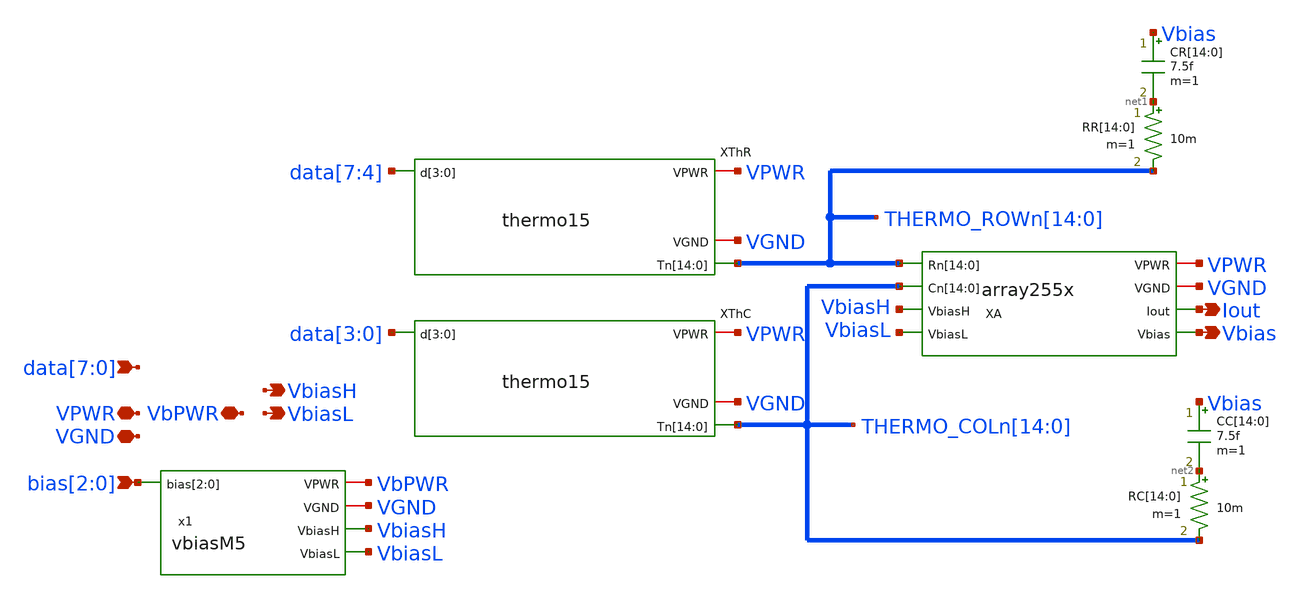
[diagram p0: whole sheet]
** sch_path: xschem-cascode-backup/csdac255.sch
**.subckt csdac255 VPWR Iout VGND bias[2],bias[1],bias[0]
*+ data[7],data[6],data[5],data[4],data[3],data[2],data[1],data[0] VbiasH VbPWR VbiasL Vbias
*.iopin VPWR
*.opin Iout
*.iopin VGND
*.ipin bias[2],bias[1],bias[0]
*.ipin data[7],data[6],data[5],data[4],data[3],data[2],data[1],data[0]
*.opin VbiasH
*.iopin VbPWR
*.opin VbiasL
*.opin Vbias
XThR VPWR VGND THERMO_ROWn[14] THERMO_ROWn[13] THERMO_ROWn[12] THERMO_ROWn[11] THERMO_ROWn[10]
+ THERMO_ROWn[9] THERMO_ROWn[8] THERMO_ROWn[7] THERMO_ROWn[6] THERMO_ROWn[5] THERMO_ROWn[4] THERMO_ROWn[3]
+ THERMO_ROWn[2] THERMO_ROWn[1] THERMO_ROWn[0] data[7] data[6] data[5] data[4] thermo15
XA VPWR VGND THERMO_ROWn[14] THERMO_ROWn[13] THERMO_ROWn[12] THERMO_ROWn[11] THERMO_ROWn[10]
+ THERMO_ROWn[9] THERMO_ROWn[8] THERMO_ROWn[7] THERMO_ROWn[6] THERMO_ROWn[5] THERMO_ROWn[4] THERMO_ROWn[3]
+ THERMO_ROWn[2] THERMO_ROWn[1] THERMO_ROWn[0] THERMO_COLn[14] THERMO_COLn[13] THERMO_COLn[12] THERMO_COLn[11]
+ THERMO_COLn[10] THERMO_COLn[9] THERMO_COLn[8] THERMO_COLn[7] THERMO_COLn[6] THERMO_COLn[5] THERMO_COLn[4]
+ THERMO_COLn[3] THERMO_COLn[2] THERMO_COLn[1] THERMO_COLn[0] VbiasH Iout Vbias VbiasL array255x
XThC VPWR VGND THERMO_COLn[14] THERMO_COLn[13] THERMO_COLn[12] THERMO_COLn[11] THERMO_COLn[10]
+ THERMO_COLn[9] THERMO_COLn[8] THERMO_COLn[7] THERMO_COLn[6] THERMO_COLn[5] THERMO_COLn[4] THERMO_COLn[3]
+ THERMO_COLn[2] THERMO_COLn[1] THERMO_COLn[0] data[3] data[2] data[1] data[0] thermo15
CR[14] Vbias net1[14] 7.5f m=1
CR[13] Vbias net1[13] 7.5f m=1
CR[12] Vbias net1[12] 7.5f m=1
CR[11] Vbias net1[11] 7.5f m=1
CR[10] Vbias net1[10] 7.5f m=1
CR[9] Vbias net1[9] 7.5f m=1
CR[8] Vbias net1[8] 7.5f m=1
CR[7] Vbias net1[7] 7.5f m=1
CR[6] Vbias net1[6] 7.5f m=1
CR[5] Vbias net1[5] 7.5f m=1
CR[4] Vbias net1[4] 7.5f m=1
CR[3] Vbias net1[3] 7.5f m=1
CR[2] Vbias net1[2] 7.5f m=1
CR[1] Vbias net1[1] 7.5f m=1
CR[0] Vbias net1[0] 7.5f m=1
RR[14] net1[14] THERMO_ROWn[14] 10m m=1
RR[13] net1[13] THERMO_ROWn[13] 10m m=1
RR[12] net1[12] THERMO_ROWn[12] 10m m=1
RR[11] net1[11] THERMO_ROWn[11] 10m m=1
RR[10] net1[10] THERMO_ROWn[10] 10m m=1
RR[9] net1[9] THERMO_ROWn[9] 10m m=1
RR[8] net1[8] THERMO_ROWn[8] 10m m=1
RR[7] net1[7] THERMO_ROWn[7] 10m m=1
RR[6] net1[6] THERMO_ROWn[6] 10m m=1
RR[5] net1[5] THERMO_ROWn[5] 10m m=1
RR[4] net1[4] THERMO_ROWn[4] 10m m=1
RR[3] net1[3] THERMO_ROWn[3] 10m m=1
RR[2] net1[2] THERMO_ROWn[2] 10m m=1
RR[1] net1[1] THERMO_ROWn[1] 10m m=1
RR[0] net1[0] THERMO_ROWn[0] 10m m=1
CC[14] Vbias net2[14] 7.5f m=1
CC[13] Vbias net2[13] 7.5f m=1
CC[12] Vbias net2[12] 7.5f m=1
CC[11] Vbias net2[11] 7.5f m=1
CC[10] Vbias net2[10] 7.5f m=1
CC[9] Vbias net2[9] 7.5f m=1
CC[8] Vbias net2[8] 7.5f m=1
CC[7] Vbias net2[7] 7.5f m=1
CC[6] Vbias net2[6] 7.5f m=1
CC[5] Vbias net2[5] 7.5f m=1
CC[4] Vbias net2[4] 7.5f m=1
CC[3] Vbias net2[3] 7.5f m=1
CC[2] Vbias net2[2] 7.5f m=1
CC[1] Vbias net2[1] 7.5f m=1
CC[0] Vbias net2[0] 7.5f m=1
RC[14] net2[14] THERMO_COLn[14] 10m m=1
RC[13] net2[13] THERMO_COLn[13] 10m m=1
RC[12] net2[12] THERMO_COLn[12] 10m m=1
RC[11] net2[11] THERMO_COLn[11] 10m m=1
RC[10] net2[10] THERMO_COLn[10] 10m m=1
RC[9] net2[9] THERMO_COLn[9] 10m m=1
RC[8] net2[8] THERMO_COLn[8] 10m m=1
RC[7] net2[7] THERMO_COLn[7] 10m m=1
RC[6] net2[6] THERMO_COLn[6] 10m m=1
RC[5] net2[5] THERMO_COLn[5] 10m m=1
RC[4] net2[4] THERMO_COLn[4] 10m m=1
RC[3] net2[3] THERMO_COLn[3] 10m m=1
RC[2] net2[2] THERMO_COLn[2] 10m m=1
RC[1] net2[1] THERMO_COLn[1] 10m m=1
RC[0] net2[0] THERMO_COLn[0] 10m m=1
x1 VbPWR VGND bias[2] bias[1] bias[0] VbiasH VbiasL vbiasM5
**.ends
.end
